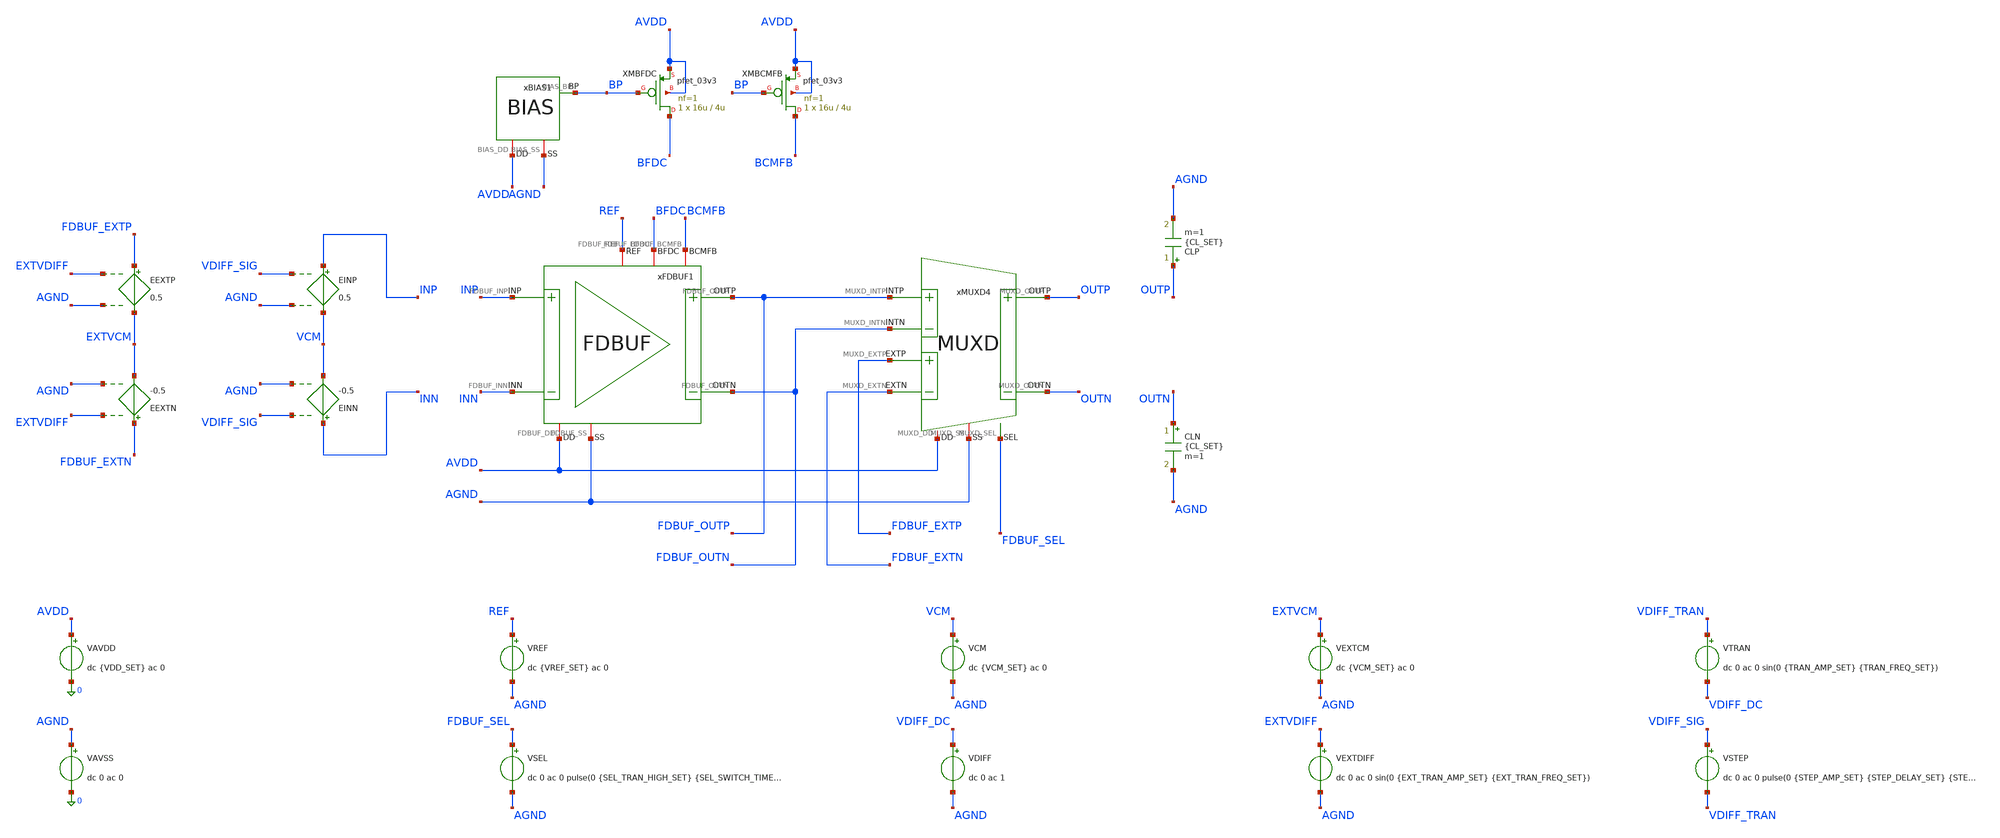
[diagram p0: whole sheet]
** sch_path: Design_Files/IC Design/Testbench/AFE_BLOCKS/FDBUF/FDBUF_TB_PVT_NOM.sch
**.subckt FDBUF_TB_PVT_NOM
CLP OUTP AGND {CL_SET} m=1
CLN OUTN AGND {CL_SET} m=1
xBIAS1 AVDD AGND BP BIAS
XMBFDC BFDC BP AVDD AVDD pfet_03v3 L=4u W=16u nf=1 ad='int((nf+1)/2) * W/nf * 0.18u' as='int((nf+2)/2) * W/nf * 0.18u'
+ pd='2*int((nf+1)/2) * (W/nf + 0.18u)' ps='2*int((nf+2)/2) * (W/nf + 0.18u)' nrd='0.18u / W' nrs='0.18u / W'
+ sa=0 sb=0 sd=0 m=1
XMBCMFB BCMFB BP AVDD AVDD pfet_03v3 L=4u W=16u nf=1 ad='int((nf+1)/2) * W/nf * 0.18u' as='int((nf+2)/2) * W/nf * 0.18u'
+ pd='2*int((nf+1)/2) * (W/nf + 0.18u)' ps='2*int((nf+2)/2) * (W/nf + 0.18u)' nrd='0.18u / W' nrs='0.18u / W'
+ sa=0 sb=0 sd=0 m=1
VAVDD AVDD 0 dc {VDD_SET} ac 0
.save i(vavdd)
VAVSS AGND 0 dc 0 ac 0
xFDBUF1 AVDD AGND INP INN FDBUF_OUTN BFDC FDBUF_OUTP BCMFB REF FDBUF
xMUXD4 AVDD AGND FDBUF_OUTP FDBUF_OUTN OUTN OUTP FDBUF_EXTP FDBUF_EXTN FDBUF_SEL MUXD
VCM VCM AGND dc {VCM_SET} ac 0
VDIFF VDIFF_DC AGND dc 0 ac 1
VREF REF AGND dc {VREF_SET} ac 0
VSEL FDBUF_SEL AGND dc 0 ac 0 pulse(0 {SEL_TRAN_HIGH_SET} {SEL_SWITCH_TIME_SET} 1u 1u 400m 800m)
VEXTCM EXTVCM AGND dc {VCM_SET} ac 0
VEXTDIFF EXTVDIFF AGND dc 0 ac 0 sin(0 {EXT_TRAN_AMP_SET} {EXT_TRAN_FREQ_SET})
EINP INP VCM VDIFF_SIG AGND 0.5
EINN INN VCM VDIFF_SIG AGND -0.5
EEXTP FDBUF_EXTP EXTVCM EXTVDIFF AGND 0.5
EEXTN FDBUF_EXTN EXTVCM EXTVDIFF AGND -0.5
VTRAN VDIFF_TRAN VDIFF_DC dc 0 ac 0 sin(0 {TRAN_AMP_SET} {TRAN_FREQ_SET})
VSTEP VDIFF_SIG VDIFF_TRAN dc 0 ac 0 pulse(0 {STEP_AMP_SET} {STEP_DELAY_SET} {STEP_TR_SET} {STEP_TF_SET}
+ {STEP_PW_SET} {STEP_PERIOD_SET})
**** begin user architecture code

* {MODELS_START}
.include $::180MCU_MODELS/design.ngspice

.param sw_stat_global=0
.param sw_stat_mismatch=0

.lib $::180MCU_MODELS/sm141064.ngspice typical
.lib $::180MCU_MODELS/sm141064.ngspice res_typical
.lib $::180MCU_MODELS/sm141064.ngspice mimcap_typical
.lib $::180MCU_MODELS/sm141064.ngspice cap_mim
.lib $::180MCU_MODELS/sm141064.ngspice bjt_typical

.csparam PROC_ID=0
* {MODELS_END}



* {SETUP_START}
.param VDD_SET=3.3
.param TEMP_SET=27

.param VCM_SET={VDD_SET/2}
.param VREF_SET={VDD_SET/2}

.param CL_SET=60p

.param FDBUF_GAIN_TARGET_SET=1

.param TRAN_AMP_SET=0
.param TRAN_FREQ_SET=10

.param STEP_AMP_SET=0
.param STEP_DELAY_SET=20u
.param STEP_TR_SET=10n
.param STEP_TF_SET=10n
.param STEP_PW_SET=100u
.param STEP_PERIOD_SET=200u

.param EXT_TRAN_AMP_SET=0
.param EXT_TRAN_FREQ_SET=25

.param SEL_TRAN_HIGH_SET=0
.param SEL_SWITCH_TIME_SET=200m

.csparam MC_RUNS=200

.temp {TEMP_SET}

.options gmin=1e-12
.options rshunt=1e12
.options method=gear
* {SETUP_END}




* {MEAS_START}
.control

destroy all

set noaskquit
set wr_singlescale
unset wr_vecnames

option klu
option numdgt=15
option method=gear
option maxord=2
option plotwinsize=0

if $&PROC_ID = 0
set proc=NOM
else
if $&PROC_ID = 1
set proc=FF
else
if $&PROC_ID = 2
set proc=SS
else
if $&PROC_ID = 3
set proc=FS
else
set proc=SF
end
end
end
end

shell mkdir -p /foss/designs/ECG_Acquisition_IC/Measurement_Results/IC_Simulation/AFE_BLOCKS/FDBUF/{$proc}.Result_txt
shell rm -f /foss/designs/ECG_Acquisition_IC/Measurement_Results/IC_Simulation/AFE_BLOCKS/FDBUF/{$proc}.Result_txt/{$proc}.*.txt

foreach vddval 3.3 3.0 3.6
foreach tval 27 -40 125

if $vddval = 3.3
if $tval = 27
set env=nom
else
if $tval = -40
set env=tl
else
set env=th
end
end
else
if $vddval = 3.0
if $tval = 27
set env=vl
else
if $tval = -40
set env=vltl
else
set env=vlth
end
end
else
if $tval = 27
set env=vh
else
if $tval = -40
set env=vhtl
else
set env=vhth
end
end
end
end

alterparam VDD_SET=$vddval
alterparam TEMP_SET=$tval

alterparam TRAN_AMP_SET=0
alterparam STEP_AMP_SET=0
alterparam EXT_TRAN_AMP_SET=0
alterparam SEL_TRAN_HIGH_SET=0

foreach lcode 0 1 2 3

if $lcode = 0
set ltag=l40
set cload=40p
else
if $lcode = 1
set ltag=l60
set cload=60p
else
if $lcode = 2
set ltag=l80
set cload=80p
else
set ltag=l100
set cload=100p
end
end
end

reset

alter CLP $cload
alter CLN $cload

alter @VSEL[DC]=0
alter @VDIFF[DC]=0

alter @VDIFF[ACMAG]=0
alter @VCM[ACMAG]=0
alter @VREF[ACMAG]=0
alter @VEXTDIFF[ACMAG]=0
alter @VAVDD[ACMAG]=0
alter @VAVSS[ACMAG]=0

save all
save @m.xmbfdc.m0[id]
save @m.xmbcmfb.m0[id]

* OFFSET

dc VDIFF -20m 20m 10u

let buffer_diff=v(FDBUF_OUTP)-v(FDBUF_OUTN)

meas dc vos_meas when buffer_diff=0 cross=1

set vos_val=$&vos_meas

echo $vos_val > /foss/designs/ECG_Acquisition_IC/Measurement_Results/IC_Simulation/AFE_BLOCKS/FDBUF/{$proc}.Result_txt/{$proc}.vos_{$ltag}_{$env}.txt

destroy all

alter @VDIFF[DC]=$vos_val

* OP

op

let op_index=0

let vdd=v(AVDD)-v(AGND)
let vref=v(REF)-v(AGND)

let vin_cm=0.5*(v(INP)+v(INN))-v(AGND)
let vin_diff=v(INP)-v(INN)

let buffer_out_cm=0.5*(v(FDBUF_OUTP)+v(FDBUF_OUTN))-v(AGND)
let buffer_out_diff=v(FDBUF_OUTP)-v(FDBUF_OUTN)
let buffer_cm_error=buffer_out_cm-vref

let out_cm=0.5*(v(OUTP)+v(OUTN))-v(AGND)
let out_diff=v(OUTP)-v(OUTN)

let idd_total=abs(vavdd#branch)
let power_total=vdd*idd_total

let ibfdc=abs(@m.xmbfdc.m0[id])
let ibcmfb=abs(@m.xmbcmfb.m0[id])

setscale op_index

wrdata /foss/designs/ECG_Acquisition_IC/Measurement_Results/IC_Simulation/AFE_BLOCKS/FDBUF/{$proc}.Result_txt/{$proc}.op_{$ltag}_{$env}.txt
+ vdd vref vin_cm vin_diff buffer_out_cm buffer_out_diff buffer_cm_error out_cm out_diff idd_total power_total
+ ibfdc ibcmfb

destroy all

* DIFF AC

alter @VDIFF[ACMAG]=1
alter @VCM[ACMAG]=0
alter @VREF[ACMAG]=0
alter @VEXTDIFF[ACMAG]=0
alter @VAVDD[ACMAG]=0
alter @VAVSS[ACMAG]=0

ac dec 150 0.01 100Meg

let vin_diff=v(INP)-v(INN)
let buffer_diff=v(FDBUF_OUTP)-v(FDBUF_OUTN)
let out_diff=v(OUTP)-v(OUTN)

let vin_r=real(vin_diff)
let vin_i=imag(vin_diff)

let buffer_r=real(buffer_diff)
let buffer_i=imag(buffer_diff)

let out_r=real(out_diff)
let out_i=imag(out_diff)

setscale frequency

wrdata /foss/designs/ECG_Acquisition_IC/Measurement_Results/IC_Simulation/AFE_BLOCKS/FDBUF/{$proc}.Result_txt/{$proc}.diff_ac_{$ltag}_{$env}.txt
+ vin_r vin_i buffer_r buffer_i out_r out_i

destroy all

* CMRR

alter @VDIFF[ACMAG]=0
alter @VCM[ACMAG]=1
alter @VREF[ACMAG]=0
alter @VEXTDIFF[ACMAG]=0
alter @VAVDD[ACMAG]=0
alter @VAVSS[ACMAG]=0

ac dec 100 0.01 1Meg

let vin_cm=0.5*(v(INP)+v(INN))-v(AGND)
let buffer_diff=v(FDBUF_OUTP)-v(FDBUF_OUTN)

let vin_r=real(vin_cm)
let vin_i=imag(vin_cm)

let out_r=real(buffer_diff)
let out_i=imag(buffer_diff)

setscale frequency

wrdata /foss/designs/ECG_Acquisition_IC/Measurement_Results/IC_Simulation/AFE_BLOCKS/FDBUF/{$proc}.Result_txt/{$proc}.cmrr_ac_{$ltag}_{$env}.txt
+ vin_r vin_i out_r out_i

destroy all

* PSRR+

alter @VDIFF[ACMAG]=0
alter @VCM[ACMAG]=0
alter @VREF[ACMAG]=0
alter @VEXTDIFF[ACMAG]=0
alter @VAVDD[ACMAG]=1
alter @VAVDD[ACPHASE]=0
alter @VAVSS[ACMAG]=0

ac dec 100 0.01 1Meg

let vsup=v(AVDD)-v(AGND)
let buffer_diff=v(FDBUF_OUTP)-v(FDBUF_OUTN)

let vsup_r=real(vsup)
let vsup_i=imag(vsup)

let out_r=real(buffer_diff)
let out_i=imag(buffer_diff)

setscale frequency

wrdata /foss/designs/ECG_Acquisition_IC/Measurement_Results/IC_Simulation/AFE_BLOCKS/FDBUF/{$proc}.Result_txt/{$proc}.psrrp_ac_{$ltag}_{$env}.txt
+ vsup_r vsup_i out_r out_i

destroy all

* PSRR-

alter @VDIFF[ACMAG]=0
alter @VCM[ACMAG]=0
alter @VREF[ACMAG]=0
alter @VEXTDIFF[ACMAG]=0
alter @VAVDD[ACMAG]=0
alter @VAVSS[ACMAG]=1
alter @VAVSS[ACPHASE]=0

ac dec 100 0.01 1Meg

let vsup=v(AVDD)-v(AGND)
let buffer_diff=v(FDBUF_OUTP)-v(FDBUF_OUTN)

let vsup_r=real(vsup)
let vsup_i=imag(vsup)

let out_r=real(buffer_diff)
let out_i=imag(buffer_diff)

setscale frequency

wrdata /foss/designs/ECG_Acquisition_IC/Measurement_Results/IC_Simulation/AFE_BLOCKS/FDBUF/{$proc}.Result_txt/{$proc}.psrrn_ac_{$ltag}_{$env}.txt
+ vsup_r vsup_i out_r out_i

destroy all

* NOISE

alter @VDIFF[ACMAG]=1
alter @VCM[ACMAG]=0
alter @VREF[ACMAG]=0
alter @VEXTDIFF[ACMAG]=0
alter @VAVDD[ACMAG]=0
alter @VAVSS[ACMAG]=0

noise v(FDBUF_OUTP,FDBUF_OUTN) VDIFF dec 100 0.01 10k

setplot previous
setscale frequency

wrdata /foss/designs/ECG_Acquisition_IC/Measurement_Results/IC_Simulation/AFE_BLOCKS/FDBUF/{$proc}.Result_txt/{$proc}.noise_{$ltag}_{$env}.txt
+ onoise_spectrum inoise_spectrum

destroy all

* SETTLING
* 100 mV differential step

alterparam TRAN_AMP_SET=0
alterparam STEP_AMP_SET=100m

reset

alter CLP $cload
alter CLN $cload

alter @VSEL[DC]=0

save all

tran 20n 150u

let vin_diff=v(INP)-v(INN)
let buffer_diff=v(FDBUF_OUTP)-v(FDBUF_OUTN)
let out_diff=v(OUTP)-v(OUTN)

setscale time

wrdata /foss/designs/ECG_Acquisition_IC/Measurement_Results/IC_Simulation/AFE_BLOCKS/FDBUF/{$proc}.Result_txt/{$proc}.settling_{$ltag}_{$env}.txt
+ vin_diff buffer_diff out_diff

destroy all

alterparam STEP_AMP_SET=0

end

end
end

* SEL
* NOM / 3.3 V / 27 C / 60 pF

if $&PROC_ID = 0

alterparam VDD_SET=3.3
alterparam TEMP_SET=27

alterparam TRAN_AMP_SET=50m
alterparam TRAN_FREQ_SET=10

alterparam STEP_AMP_SET=0

alterparam EXT_TRAN_AMP_SET=50m
alterparam EXT_TRAN_FREQ_SET=25

alterparam SEL_TRAN_HIGH_SET=3.3
alterparam SEL_SWITCH_TIME_SET=200m

reset

alter CLP 60p
alter CLN 60p

save all

tran 20u 400m

let int_diff=v(FDBUF_OUTP)-v(FDBUF_OUTN)
let ext_diff=v(FDBUF_EXTP)-v(FDBUF_EXTN)
let out_diff=v(OUTP)-v(OUTN)

setscale time

wrdata /foss/designs/ECG_Acquisition_IC/Measurement_Results/IC_Simulation/AFE_BLOCKS/FDBUF/{$proc}.Result_txt/{$proc}.sel_tran_nom.txt
+ v(FDBUF_SEL) int_diff ext_diff out_diff

destroy all

end

quit

.endc
* {MEAS_END}


**** end user architecture code
**.ends
.end
